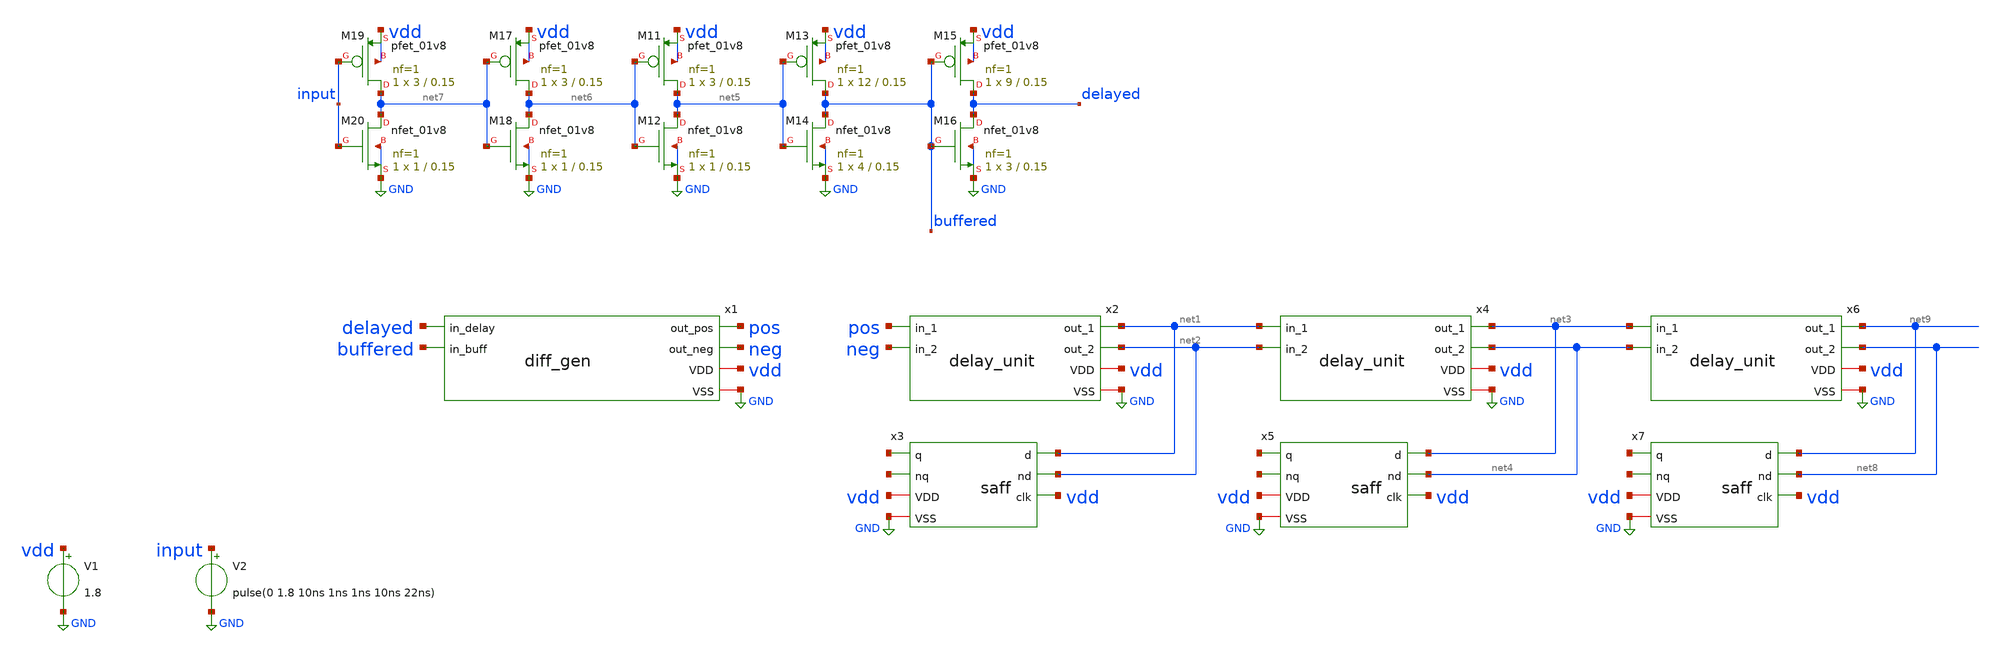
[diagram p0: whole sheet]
** sch_path: xschem/diff_gen_tb.sch
**.subckt diff_gen_tb
x1 delayed buffered pos neg vdd GND diff_gen
V1 vdd GND 1.8
V2 input GND pulse(0 1.8 10ns 1ns 1ns 10ns 22ns)
x2 net1 pos neg vdd net2 GND delay_unit
x3 net1 net2 vdd net10 net11 vdd GND saff
x4 net3 net1 net2 vdd net4 GND delay_unit
x5 net3 net4 vdd net12 net13 vdd GND saff
x6 net9 net3 net4 vdd net8 GND delay_unit
x7 net9 net8 vdd net14 net15 vdd GND saff
XM11 net5 net6 vdd vdd sky130_fd_pr__pfet_01v8 L=0.15 W=3 nf=1 ad='int((nf+1)/2) * W/nf * 0.29' as='int((nf+2)/2) * W/nf * 0.29'
+ pd='2*int((nf+1)/2) * (W/nf + 0.29)' ps='2*int((nf+2)/2) * (W/nf + 0.29)' nrd='0.29 / W' nrs='0.29 / W'
+ sa=0 sb=0 sd=0 mult=1 m=1
XM12 net5 net6 GND GND sky130_fd_pr__nfet_01v8 L=0.15 W=1 nf=1 ad='int((nf+1)/2) * W/nf * 0.29' as='int((nf+2)/2) * W/nf * 0.29'
+ pd='2*int((nf+1)/2) * (W/nf + 0.29)' ps='2*int((nf+2)/2) * (W/nf + 0.29)' nrd='0.29 / W' nrs='0.29 / W'
+ sa=0 sb=0 sd=0 mult=1 m=1
XM13 buffered net5 vdd vdd sky130_fd_pr__pfet_01v8 L=0.15 W=12 nf=1 ad='int((nf+1)/2) * W/nf * 0.29'
+ as='int((nf+2)/2) * W/nf * 0.29' pd='2*int((nf+1)/2) * (W/nf + 0.29)' ps='2*int((nf+2)/2) * (W/nf + 0.29)'
+ nrd='0.29 / W' nrs='0.29 / W' sa=0 sb=0 sd=0 mult=1 m=1
XM14 buffered net5 GND GND sky130_fd_pr__nfet_01v8 L=0.15 W=4 nf=1 ad='int((nf+1)/2) * W/nf * 0.29' as='int((nf+2)/2) * W/nf * 0.29'
+ pd='2*int((nf+1)/2) * (W/nf + 0.29)' ps='2*int((nf+2)/2) * (W/nf + 0.29)' nrd='0.29 / W' nrs='0.29 / W'
+ sa=0 sb=0 sd=0 mult=1 m=1
XM15 delayed buffered vdd vdd sky130_fd_pr__pfet_01v8 L=0.15 W=9 nf=1 ad='int((nf+1)/2) * W/nf * 0.29'
+ as='int((nf+2)/2) * W/nf * 0.29' pd='2*int((nf+1)/2) * (W/nf + 0.29)' ps='2*int((nf+2)/2) * (W/nf + 0.29)'
+ nrd='0.29 / W' nrs='0.29 / W' sa=0 sb=0 sd=0 mult=1 m=1
XM16 delayed buffered GND GND sky130_fd_pr__nfet_01v8 L=0.15 W=3 nf=1 ad='int((nf+1)/2) * W/nf * 0.29'
+ as='int((nf+2)/2) * W/nf * 0.29' pd='2*int((nf+1)/2) * (W/nf + 0.29)' ps='2*int((nf+2)/2) * (W/nf + 0.29)'
+ nrd='0.29 / W' nrs='0.29 / W' sa=0 sb=0 sd=0 mult=1 m=1
XM17 net6 net7 vdd vdd sky130_fd_pr__pfet_01v8 L=0.15 W=3 nf=1 ad='int((nf+1)/2) * W/nf * 0.29' as='int((nf+2)/2) * W/nf * 0.29'
+ pd='2*int((nf+1)/2) * (W/nf + 0.29)' ps='2*int((nf+2)/2) * (W/nf + 0.29)' nrd='0.29 / W' nrs='0.29 / W'
+ sa=0 sb=0 sd=0 mult=1 m=1
XM18 net6 net7 GND GND sky130_fd_pr__nfet_01v8 L=0.15 W=1 nf=1 ad='int((nf+1)/2) * W/nf * 0.29' as='int((nf+2)/2) * W/nf * 0.29'
+ pd='2*int((nf+1)/2) * (W/nf + 0.29)' ps='2*int((nf+2)/2) * (W/nf + 0.29)' nrd='0.29 / W' nrs='0.29 / W'
+ sa=0 sb=0 sd=0 mult=1 m=1
XM19 net7 input vdd vdd sky130_fd_pr__pfet_01v8 L=0.15 W=3 nf=1 ad='int((nf+1)/2) * W/nf * 0.29' as='int((nf+2)/2) * W/nf * 0.29'
+ pd='2*int((nf+1)/2) * (W/nf + 0.29)' ps='2*int((nf+2)/2) * (W/nf + 0.29)' nrd='0.29 / W' nrs='0.29 / W'
+ sa=0 sb=0 sd=0 mult=1 m=1
XM20 net7 input GND GND sky130_fd_pr__nfet_01v8 L=0.15 W=1 nf=1 ad='int((nf+1)/2) * W/nf * 0.29' as='int((nf+2)/2) * W/nf * 0.29'
+ pd='2*int((nf+1)/2) * (W/nf + 0.29)' ps='2*int((nf+2)/2) * (W/nf + 0.29)' nrd='0.29 / W' nrs='0.29 / W'
+ sa=0 sb=0 sd=0 mult=1 m=1
**** begin user architecture code

** opencircuitdesign pdks install
.lib $::SKYWATER_MODELS/sky130.lib.spice tt





.tran 0.001n 50n
.save v(buffered) v(delayed) v(pos) v(neg)

.control
run
set wr_vecnames
wrdata diff_gen_tb.txt v(buffered) v(delayed) v(pos) v(neg)
.endc


**** end user architecture code
**.ends

* expanding   symbol:  diff_gen.sym # of pins=6
** sym_path: xschem/diff_gen.sym
** sch_path: xschem/diff_gen.sch
.subckt diff_gen in_delay in_buff out_pos out_neg VDD VSS
*.iopin VDD
*.iopin VSS
*.ipin in_delay
*.opin out_pos
*.ipin in_buff
*.opin out_neg
x1 out_1_1 in_buff in_delay VDD out_2_1 VSS delay_unit
x2 out_1_2 out_1_1 out_2_1 VDD out_2_2 VSS delay_unit
x3 out_1_3 out_1_2 out_2_2 VDD out_2_3 VSS delay_unit
x4 out_1_4 out_1_3 out_2_3 VDD out_2_4 VSS delay_unit
x5 out_1_5 out_1_4 out_2_4 VDD out_2_5 VSS delay_unit
x6 out_1_6 out_1_5 out_2_5 VDD out_2_6 VSS delay_unit
x7 out_pos out_1_6 out_2_6 VDD out_neg VSS delay_unit
.ends


* expanding   symbol:  delay_unit.sym # of pins=6
** sym_path: xschem/delay_unit.sym
** sch_path: xschem/delay_unit.sch
.subckt delay_unit out_1 in_1 in_2 VDD out_2 VSS
*.iopin VDD
*.ipin in_1
*.opin out_1
*.iopin VSS
*.ipin in_2
*.opin out_2
XM5 out_2 in_1 VDD VDD sky130_fd_pr__pfet_01v8 L=0.15 W=9 nf=1 ad='int((nf+1)/2) * W/nf * 0.29' as='int((nf+2)/2) * W/nf * 0.29'
+ pd='2*int((nf+1)/2) * (W/nf + 0.29)' ps='2*int((nf+2)/2) * (W/nf + 0.29)' nrd='0.29 / W' nrs='0.29 / W'
+ sa=0 sb=0 sd=0 mult=1 m=1
XM7 out_2 in_1 VSS VSS sky130_fd_pr__nfet_01v8 L=0.15 W=3 nf=1 ad='int((nf+1)/2) * W/nf * 0.29' as='int((nf+2)/2) * W/nf * 0.29'
+ pd='2*int((nf+1)/2) * (W/nf + 0.29)' ps='2*int((nf+2)/2) * (W/nf + 0.29)' nrd='0.29 / W' nrs='0.29 / W'
+ sa=0 sb=0 sd=0 mult=1 m=1
XM1 out_1 in_2 VDD VDD sky130_fd_pr__pfet_01v8 L=0.15 W=9 nf=1 ad='int((nf+1)/2) * W/nf * 0.29' as='int((nf+2)/2) * W/nf * 0.29'
+ pd='2*int((nf+1)/2) * (W/nf + 0.29)' ps='2*int((nf+2)/2) * (W/nf + 0.29)' nrd='0.29 / W' nrs='0.29 / W'
+ sa=0 sb=0 sd=0 mult=1 m=1
XM2 out_1 in_2 VSS VSS sky130_fd_pr__nfet_01v8 L=0.15 W=3 nf=1 ad='int((nf+1)/2) * W/nf * 0.29' as='int((nf+2)/2) * W/nf * 0.29'
+ pd='2*int((nf+1)/2) * (W/nf + 0.29)' ps='2*int((nf+2)/2) * (W/nf + 0.29)' nrd='0.29 / W' nrs='0.29 / W'
+ sa=0 sb=0 sd=0 mult=1 m=1
XM3 in_1 in_2 VDD VDD sky130_fd_pr__pfet_01v8 L=0.15 W=3 nf=1 ad='int((nf+1)/2) * W/nf * 0.29' as='int((nf+2)/2) * W/nf * 0.29'
+ pd='2*int((nf+1)/2) * (W/nf + 0.29)' ps='2*int((nf+2)/2) * (W/nf + 0.29)' nrd='0.29 / W' nrs='0.29 / W'
+ sa=0 sb=0 sd=0 mult=1 m=1
XM4 in_1 in_2 VSS VSS sky130_fd_pr__nfet_01v8 L=0.15 W=1 nf=1 ad='int((nf+1)/2) * W/nf * 0.29' as='int((nf+2)/2) * W/nf * 0.29'
+ pd='2*int((nf+1)/2) * (W/nf + 0.29)' ps='2*int((nf+2)/2) * (W/nf + 0.29)' nrd='0.29 / W' nrs='0.29 / W'
+ sa=0 sb=0 sd=0 mult=1 m=1
XM6 in_2 in_1 VDD VDD sky130_fd_pr__pfet_01v8 L=0.15 W=3 nf=1 ad='int((nf+1)/2) * W/nf * 0.29' as='int((nf+2)/2) * W/nf * 0.29'
+ pd='2*int((nf+1)/2) * (W/nf + 0.29)' ps='2*int((nf+2)/2) * (W/nf + 0.29)' nrd='0.29 / W' nrs='0.29 / W'
+ sa=0 sb=0 sd=0 mult=1 m=1
XM8 in_2 in_1 VSS VSS sky130_fd_pr__nfet_01v8 L=0.15 W=1 nf=1 ad='int((nf+1)/2) * W/nf * 0.29' as='int((nf+2)/2) * W/nf * 0.29'
+ pd='2*int((nf+1)/2) * (W/nf + 0.29)' ps='2*int((nf+2)/2) * (W/nf + 0.29)' nrd='0.29 / W' nrs='0.29 / W'
+ sa=0 sb=0 sd=0 mult=1 m=1
.ends


* expanding   symbol:  saff.sym # of pins=7
** sym_path: xschem/saff.sym
** sch_path: xschem/saff.sch
.subckt saff d nd clk q nq VDD VSS
*.iopin VDD
*.ipin d
*.opin q
*.iopin VSS
*.ipin nd
*.ipin clk
*.opin nq
XM2 net3 q VSS VSS sky130_fd_pr__nfet_01v8 L=0.15 W=1 nf=1 ad='int((nf+1)/2) * W/nf * 0.29' as='int((nf+2)/2) * W/nf * 0.29'
+ pd='2*int((nf+1)/2) * (W/nf + 0.29)' ps='2*int((nf+2)/2) * (W/nf + 0.29)' nrd='0.29 / W' nrs='0.29 / W'
+ sa=0 sb=0 sd=0 mult=1 m=1
XM3 left_latch_1 clk VDD VDD sky130_fd_pr__pfet_01v8 L=0.15 W=3 nf=1 ad='int((nf+1)/2) * W/nf * 0.29'
+ as='int((nf+2)/2) * W/nf * 0.29' pd='2*int((nf+1)/2) * (W/nf + 0.29)' ps='2*int((nf+2)/2) * (W/nf + 0.29)'
+ nrd='0.29 / W' nrs='0.29 / W' sa=0 sb=0 sd=0 mult=1 m=1
XM4 right_latch_1 clk VDD VDD sky130_fd_pr__pfet_01v8 L=0.15 W=3 nf=1 ad='int((nf+1)/2) * W/nf * 0.29'
+ as='int((nf+2)/2) * W/nf * 0.29' pd='2*int((nf+1)/2) * (W/nf + 0.29)' ps='2*int((nf+2)/2) * (W/nf + 0.29)'
+ nrd='0.29 / W' nrs='0.29 / W' sa=0 sb=0 sd=0 mult=1 m=1
XM5 right_latch_1 left_latch_1 VDD VDD sky130_fd_pr__pfet_01v8 L=0.15 W=3 nf=1 ad='int((nf+1)/2) * W/nf * 0.29'
+ as='int((nf+2)/2) * W/nf * 0.29' pd='2*int((nf+1)/2) * (W/nf + 0.29)' ps='2*int((nf+2)/2) * (W/nf + 0.29)'
+ nrd='0.29 / W' nrs='0.29 / W' sa=0 sb=0 sd=0 mult=1 m=1
XM6 left_latch_1 right_latch_1 VDD VDD sky130_fd_pr__pfet_01v8 L=0.15 W=3 nf=1 ad='int((nf+1)/2) * W/nf * 0.29'
+ as='int((nf+2)/2) * W/nf * 0.29' pd='2*int((nf+1)/2) * (W/nf + 0.29)' ps='2*int((nf+2)/2) * (W/nf + 0.29)'
+ nrd='0.29 / W' nrs='0.29 / W' sa=0 sb=0 sd=0 mult=1 m=1
XM7 right_latch_1 left_latch_1 net7 VSS sky130_fd_pr__nfet_01v8 L=0.15 W=6 nf=1 ad='int((nf+1)/2) * W/nf * 0.29'
+ as='int((nf+2)/2) * W/nf * 0.29' pd='2*int((nf+1)/2) * (W/nf + 0.29)' ps='2*int((nf+2)/2) * (W/nf + 0.29)'
+ nrd='0.29 / W' nrs='0.29 / W' sa=0 sb=0 sd=0 mult=1 m=1
XM8 left_latch_1 right_latch_1 net5 VSS sky130_fd_pr__nfet_01v8 L=0.15 W=6 nf=1 ad='int((nf+1)/2) * W/nf * 0.29'
+ as='int((nf+2)/2) * W/nf * 0.29' pd='2*int((nf+1)/2) * (W/nf + 0.29)' ps='2*int((nf+2)/2) * (W/nf + 0.29)'
+ nrd='0.29 / W' nrs='0.29 / W' sa=0 sb=0 sd=0 mult=1 m=1
XM9 net6 clk VSS VSS sky130_fd_pr__nfet_01v8 L=0.15 W=15 nf=1 ad='int((nf+1)/2) * W/nf * 0.29' as='int((nf+2)/2) * W/nf * 0.29'
+ pd='2*int((nf+1)/2) * (W/nf + 0.29)' ps='2*int((nf+2)/2) * (W/nf + 0.29)' nrd='0.29 / W' nrs='0.29 / W'
+ sa=0 sb=0 sd=0 mult=1 m=1
XM10 net7 nd net6 VSS sky130_fd_pr__nfet_01v8 L=0.15 W=12 nf=1 ad='int((nf+1)/2) * W/nf * 0.29' as='int((nf+2)/2) * W/nf * 0.29'
+ pd='2*int((nf+1)/2) * (W/nf + 0.29)' ps='2*int((nf+2)/2) * (W/nf + 0.29)' nrd='0.29 / W' nrs='0.29 / W'
+ sa=0 sb=0 sd=0 mult=1 m=1
XM11 net5 d net6 VSS sky130_fd_pr__nfet_01v8 L=0.15 W=12 nf=1 ad='int((nf+1)/2) * W/nf * 0.29' as='int((nf+2)/2) * W/nf * 0.29'
+ pd='2*int((nf+1)/2) * (W/nf + 0.29)' ps='2*int((nf+2)/2) * (W/nf + 0.29)' nrd='0.29 / W' nrs='0.29 / W'
+ sa=0 sb=0 sd=0 mult=1 m=1
XM12 right_latch_2 left_latch_1 VDD VDD sky130_fd_pr__pfet_01v8 L=0.15 W=6 nf=1 ad='int((nf+1)/2) * W/nf * 0.29'
+ as='int((nf+2)/2) * W/nf * 0.29' pd='2*int((nf+1)/2) * (W/nf + 0.29)' ps='2*int((nf+2)/2) * (W/nf + 0.29)'
+ nrd='0.29 / W' nrs='0.29 / W' sa=0 sb=0 sd=0 mult=1 m=1
XM13 right_latch_2 left_latch_1 VSS VSS sky130_fd_pr__nfet_01v8 L=0.15 W=2 nf=1 ad='int((nf+1)/2) * W/nf * 0.29'
+ as='int((nf+2)/2) * W/nf * 0.29' pd='2*int((nf+1)/2) * (W/nf + 0.29)' ps='2*int((nf+2)/2) * (W/nf + 0.29)'
+ nrd='0.29 / W' nrs='0.29 / W' sa=0 sb=0 sd=0 mult=1 m=1
XM14 left_latch_2 right_latch_1 VDD VDD sky130_fd_pr__pfet_01v8 L=0.15 W=6 nf=1 ad='int((nf+1)/2) * W/nf * 0.29'
+ as='int((nf+2)/2) * W/nf * 0.29' pd='2*int((nf+1)/2) * (W/nf + 0.29)' ps='2*int((nf+2)/2) * (W/nf + 0.29)'
+ nrd='0.29 / W' nrs='0.29 / W' sa=0 sb=0 sd=0 mult=1 m=1
XM15 left_latch_2 right_latch_1 VSS VSS sky130_fd_pr__nfet_01v8 L=0.15 W=2 nf=1 ad='int((nf+1)/2) * W/nf * 0.29'
+ as='int((nf+2)/2) * W/nf * 0.29' pd='2*int((nf+1)/2) * (W/nf + 0.29)' ps='2*int((nf+2)/2) * (W/nf + 0.29)'
+ nrd='0.29 / W' nrs='0.29 / W' sa=0 sb=0 sd=0 mult=1 m=1
XM16 q left_latch_1 VDD VDD sky130_fd_pr__pfet_01v8 L=0.15 W=3 nf=1 ad='int((nf+1)/2) * W/nf * 0.29'
+ as='int((nf+2)/2) * W/nf * 0.29' pd='2*int((nf+1)/2) * (W/nf + 0.29)' ps='2*int((nf+2)/2) * (W/nf + 0.29)'
+ nrd='0.29 / W' nrs='0.29 / W' sa=0 sb=0 sd=0 mult=1 m=1
XM17 q left_latch_2 VSS VSS sky130_fd_pr__nfet_01v8 L=0.15 W=1 nf=1 ad='int((nf+1)/2) * W/nf * 0.29'
+ as='int((nf+2)/2) * W/nf * 0.29' pd='2*int((nf+1)/2) * (W/nf + 0.29)' ps='2*int((nf+2)/2) * (W/nf + 0.29)'
+ nrd='0.29 / W' nrs='0.29 / W' sa=0 sb=0 sd=0 mult=1 m=1
XM18 nq right_latch_1 VDD VDD sky130_fd_pr__pfet_01v8 L=0.15 W=3 nf=1 ad='int((nf+1)/2) * W/nf * 0.29'
+ as='int((nf+2)/2) * W/nf * 0.29' pd='2*int((nf+1)/2) * (W/nf + 0.29)' ps='2*int((nf+2)/2) * (W/nf + 0.29)'
+ nrd='0.29 / W' nrs='0.29 / W' sa=0 sb=0 sd=0 mult=1 m=1
XM19 nq right_latch_2 VSS VSS sky130_fd_pr__nfet_01v8 L=0.15 W=1 nf=1 ad='int((nf+1)/2) * W/nf * 0.29'
+ as='int((nf+2)/2) * W/nf * 0.29' pd='2*int((nf+1)/2) * (W/nf + 0.29)' ps='2*int((nf+2)/2) * (W/nf + 0.29)'
+ nrd='0.29 / W' nrs='0.29 / W' sa=0 sb=0 sd=0 mult=1 m=1
XM20 net2 q VDD VDD sky130_fd_pr__pfet_01v8 L=0.15 W=3 nf=1 ad='int((nf+1)/2) * W/nf * 0.29' as='int((nf+2)/2) * W/nf * 0.29'
+ pd='2*int((nf+1)/2) * (W/nf + 0.29)' ps='2*int((nf+2)/2) * (W/nf + 0.29)' nrd='0.29 / W' nrs='0.29 / W'
+ sa=0 sb=0 sd=0 mult=1 m=1
XM21 nq right_latch_2 net2 VDD sky130_fd_pr__pfet_01v8 L=0.15 W=3 nf=1 ad='int((nf+1)/2) * W/nf * 0.29'
+ as='int((nf+2)/2) * W/nf * 0.29' pd='2*int((nf+1)/2) * (W/nf + 0.29)' ps='2*int((nf+2)/2) * (W/nf + 0.29)'
+ nrd='0.29 / W' nrs='0.29 / W' sa=0 sb=0 sd=0 mult=1 m=1
XM22 q left_latch_2 net1 VDD sky130_fd_pr__pfet_01v8 L=0.15 W=3 nf=1 ad='int((nf+1)/2) * W/nf * 0.29'
+ as='int((nf+2)/2) * W/nf * 0.29' pd='2*int((nf+1)/2) * (W/nf + 0.29)' ps='2*int((nf+2)/2) * (W/nf + 0.29)'
+ nrd='0.29 / W' nrs='0.29 / W' sa=0 sb=0 sd=0 mult=1 m=1
XM23 net1 nq VDD VDD sky130_fd_pr__pfet_01v8 L=0.15 W=3 nf=1 ad='int((nf+1)/2) * W/nf * 0.29' as='int((nf+2)/2) * W/nf * 0.29'
+ pd='2*int((nf+1)/2) * (W/nf + 0.29)' ps='2*int((nf+2)/2) * (W/nf + 0.29)' nrd='0.29 / W' nrs='0.29 / W'
+ sa=0 sb=0 sd=0 mult=1 m=1
XM24 q left_latch_1 net4 VSS sky130_fd_pr__nfet_01v8 L=0.15 W=1 nf=1 ad='int((nf+1)/2) * W/nf * 0.29'
+ as='int((nf+2)/2) * W/nf * 0.29' pd='2*int((nf+1)/2) * (W/nf + 0.29)' ps='2*int((nf+2)/2) * (W/nf + 0.29)'
+ nrd='0.29 / W' nrs='0.29 / W' sa=0 sb=0 sd=0 mult=1 m=1
XM25 nq right_latch_1 net3 VSS sky130_fd_pr__nfet_01v8 L=0.15 W=1 nf=1 ad='int((nf+1)/2) * W/nf * 0.29'
+ as='int((nf+2)/2) * W/nf * 0.29' pd='2*int((nf+1)/2) * (W/nf + 0.29)' ps='2*int((nf+2)/2) * (W/nf + 0.29)'
+ nrd='0.29 / W' nrs='0.29 / W' sa=0 sb=0 sd=0 mult=1 m=1
XM26 net4 nq VSS VSS sky130_fd_pr__nfet_01v8 L=0.15 W=1 nf=1 ad='int((nf+1)/2) * W/nf * 0.29' as='int((nf+2)/2) * W/nf * 0.29'
+ pd='2*int((nf+1)/2) * (W/nf + 0.29)' ps='2*int((nf+2)/2) * (W/nf + 0.29)' nrd='0.29 / W' nrs='0.29 / W'
+ sa=0 sb=0 sd=0 mult=1 m=1
.ends

.GLOBAL GND
.end
